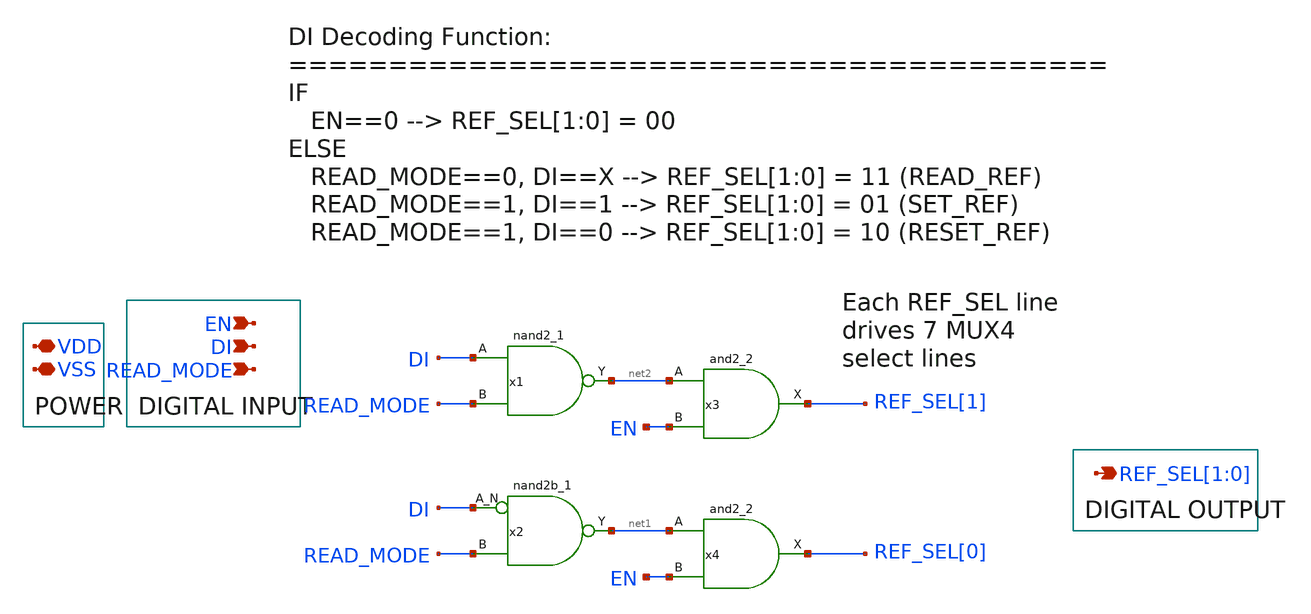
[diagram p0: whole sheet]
** sch_path: BL_Read_Interface/rram_read_di_decoding.sch
**.subckt rram_read_di_decoding EN REF_SEL[1],REF_SEL[0] VDD VSS DI READ_MODE
*.ipin EN
*.opin REF_SEL[1],REF_SEL[0]
*.iopin VDD
*.iopin VSS
*.ipin DI
*.ipin READ_MODE
x1 DI READ_MODE VSS VSS VDD VDD net2 sky130_fd_sc_hd__nand2_1
x2 DI READ_MODE VSS VSS VDD VDD net1 sky130_fd_sc_hd__nand2b_1
x3 net2 EN VSS VSS VDD VDD REF_SEL[1] sky130_fd_sc_hd__and2_2
x4 net1 EN VSS VSS VDD VDD REF_SEL[0] sky130_fd_sc_hd__and2_2
**.ends
.end
